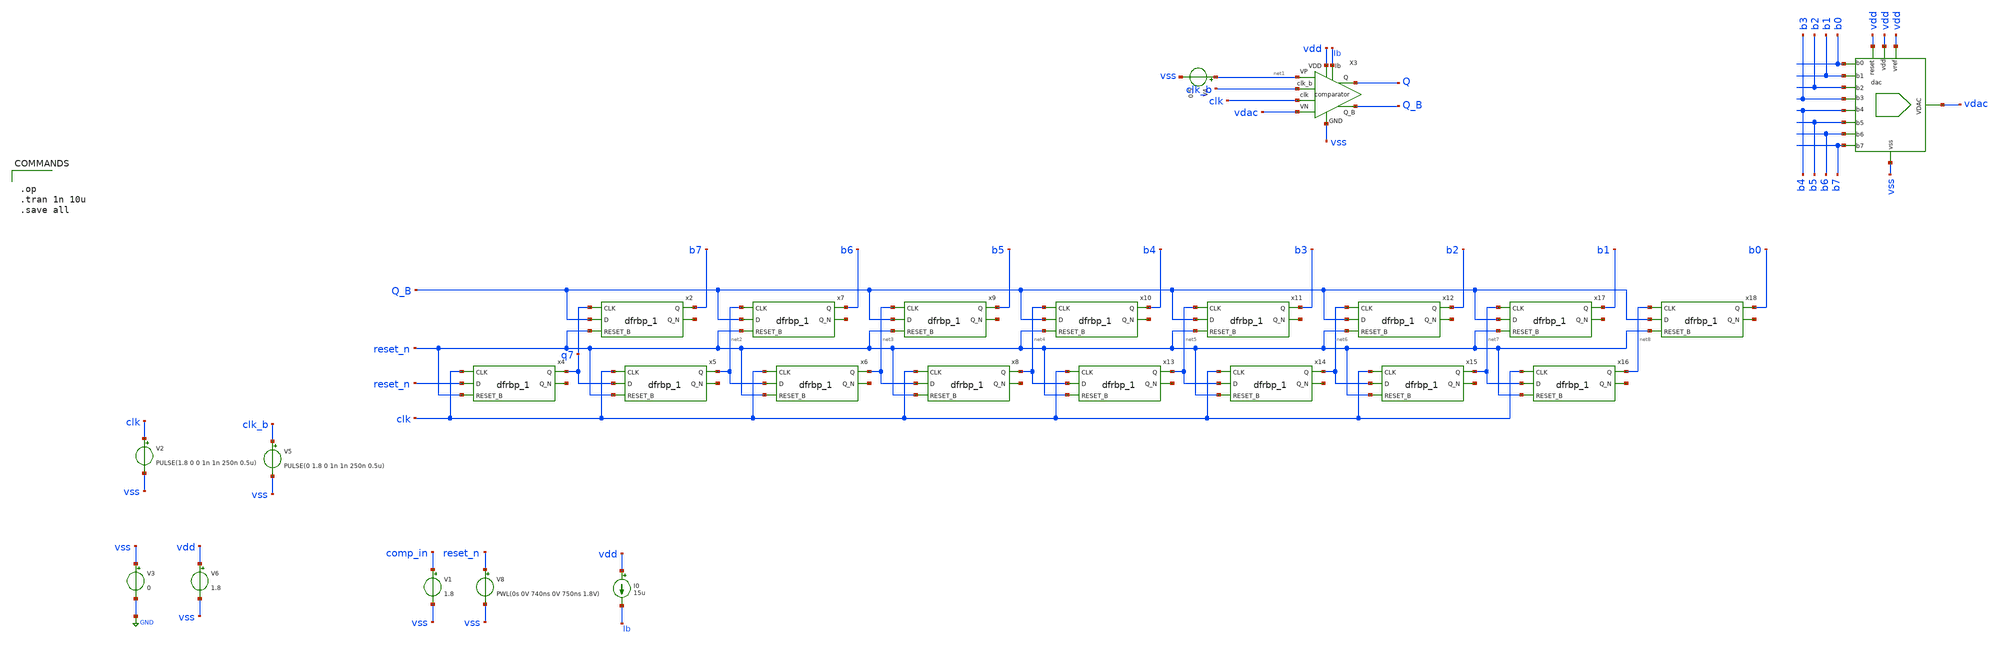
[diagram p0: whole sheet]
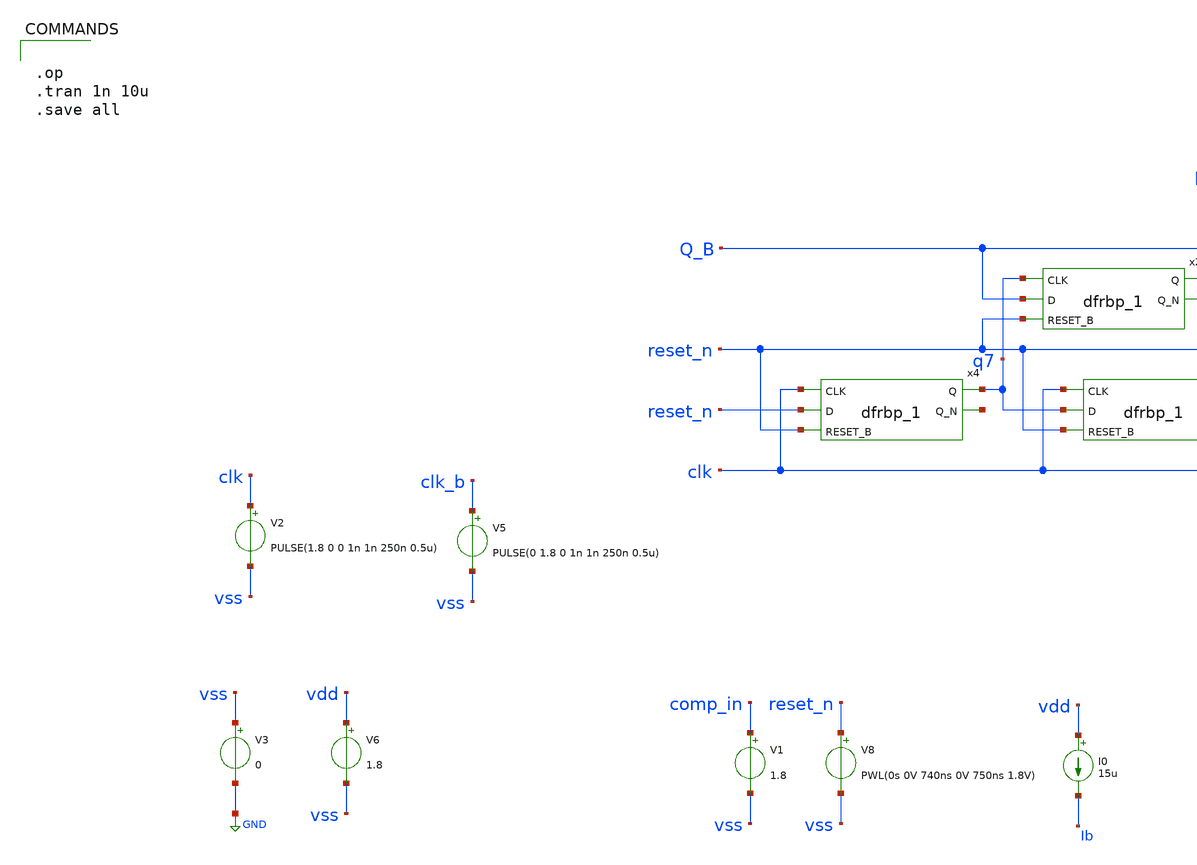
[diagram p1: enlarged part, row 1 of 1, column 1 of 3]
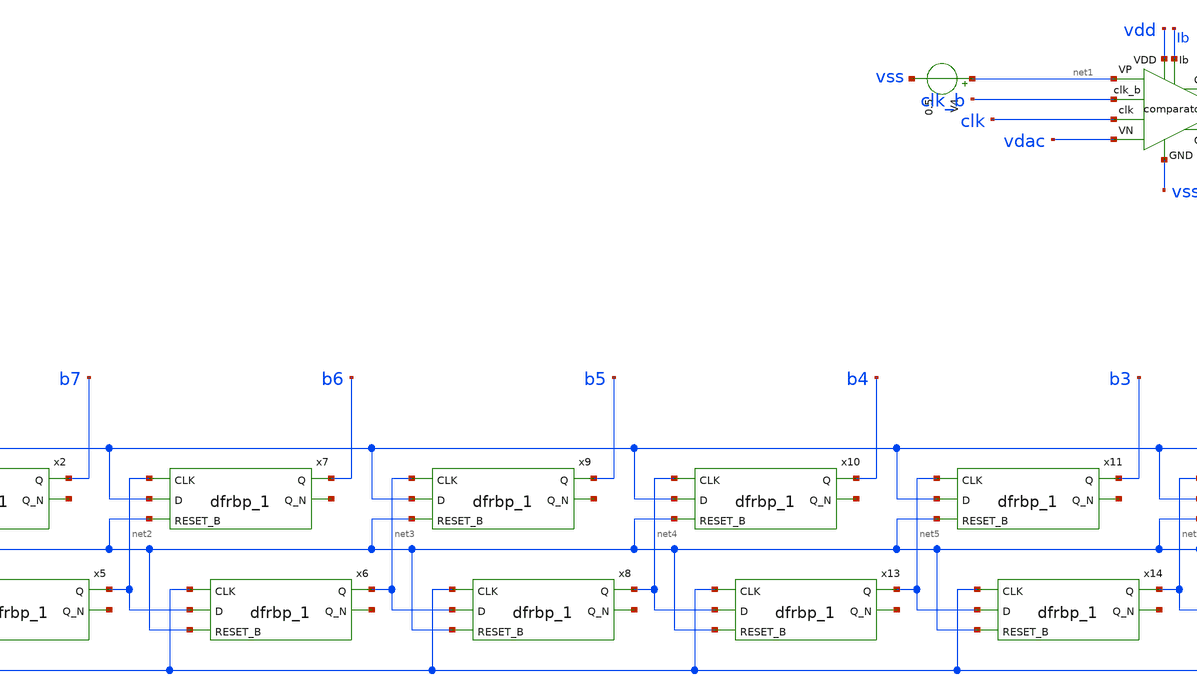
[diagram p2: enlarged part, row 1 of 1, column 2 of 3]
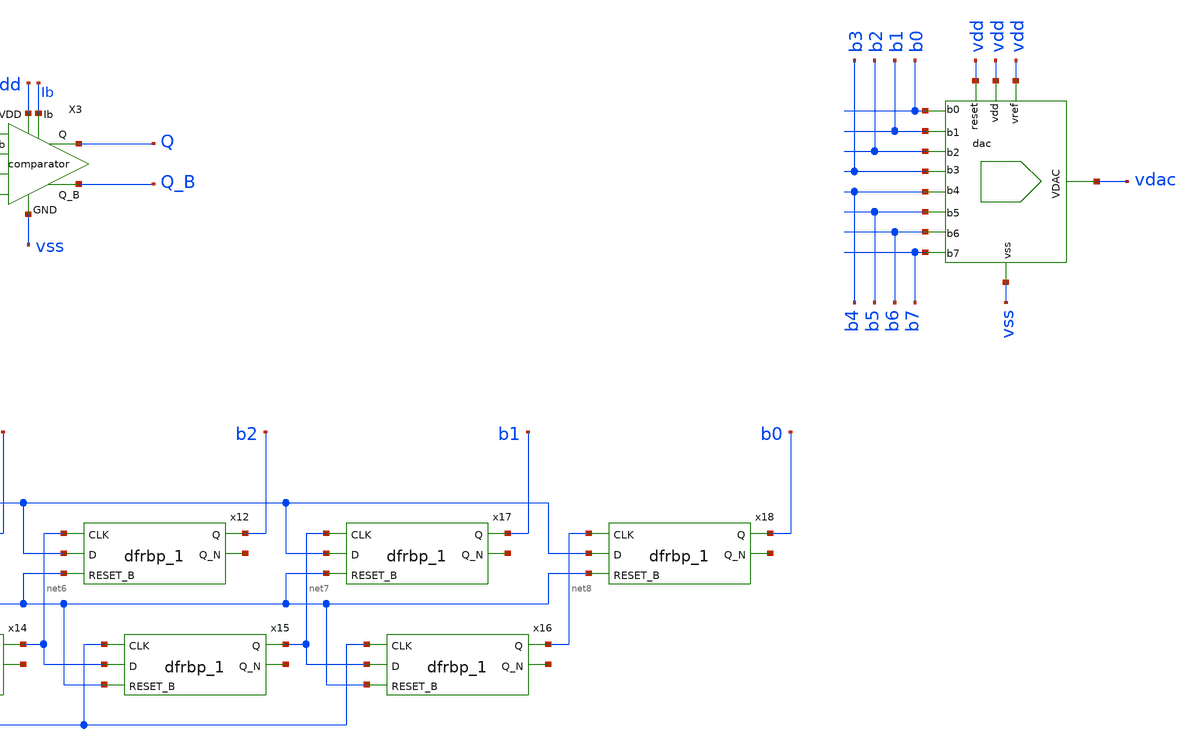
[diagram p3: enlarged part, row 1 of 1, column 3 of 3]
** sch_path: xschem/sar_logic/sar_logic_tb.sch
.lib $::SKYWATER_MODELS/sky130.lib.spice tt
.include $::SKYWATER_STDCELLS/sky130_fd_sc_hd.spice

**.subckt sar_logic_tb
V2 clk vss PULSE(1.8 0 0 1n 1n 250n 0.5u)
V1 comp_in vss 1.8
V6 vdd vss 1.8
V8 reset_n vss PWL(0s 0V 740ns 0V 750ns 1.8V)
X3 net1 vdac vss Q_B Q vdd clk Ib clk_b comparator
V4 net1 vss 0.5
I0 vdd Ib 15u
x2 q7 Q_B reset_n vss vss vdd vdd b7 net9 sky130_fd_sc_hd__dfrbp_1
x7 net2 Q_B reset_n vss vss vdd vdd b6 net10 sky130_fd_sc_hd__dfrbp_1
x4 clk reset_n reset_n vss vss vdd vdd q7 net11 sky130_fd_sc_hd__dfrbp_1
x5 clk q7 reset_n vss vss vdd vdd net2 net12 sky130_fd_sc_hd__dfrbp_1
x6 clk net2 reset_n vss vss vdd vdd net3 net13 sky130_fd_sc_hd__dfrbp_1
x8 clk net3 reset_n vss vss vdd vdd net4 net14 sky130_fd_sc_hd__dfrbp_1
x9 net3 Q_B reset_n vss vss vdd vdd b5 net15 sky130_fd_sc_hd__dfrbp_1
x10 net4 Q_B reset_n vss vss vdd vdd b4 net16 sky130_fd_sc_hd__dfrbp_1
x11 net5 Q_B reset_n vss vss vdd vdd b3 net17 sky130_fd_sc_hd__dfrbp_1
x12 net6 Q_B reset_n vss vss vdd vdd b2 net18 sky130_fd_sc_hd__dfrbp_1
x13 clk net4 reset_n vss vss vdd vdd net5 net19 sky130_fd_sc_hd__dfrbp_1
x14 clk net5 reset_n vss vss vdd vdd net6 net20 sky130_fd_sc_hd__dfrbp_1
x15 clk net6 reset_n vss vss vdd vdd net7 net21 sky130_fd_sc_hd__dfrbp_1
x16 clk net7 reset_n vss vss vdd vdd net8 net22 sky130_fd_sc_hd__dfrbp_1
x17 net7 Q_B reset_n vss vss vdd vdd b1 net23 sky130_fd_sc_hd__dfrbp_1
x18 net8 Q_B reset_n vss vss vdd vdd b0 net24 sky130_fd_sc_hd__dfrbp_1
X1 vss vdac vdd vdd b0 b1 b2 b3 b4 b5 b6 b7 vdd dac
V3 vss GND 0
V5 clk_b vss PULSE(0 1.8 0 1n 1n 250n 0.5u)
**** begin user architecture code


.op
.tran 1n 10u
.save all


**** end user architecture code
**.ends
.GLOBAL GND
.end
